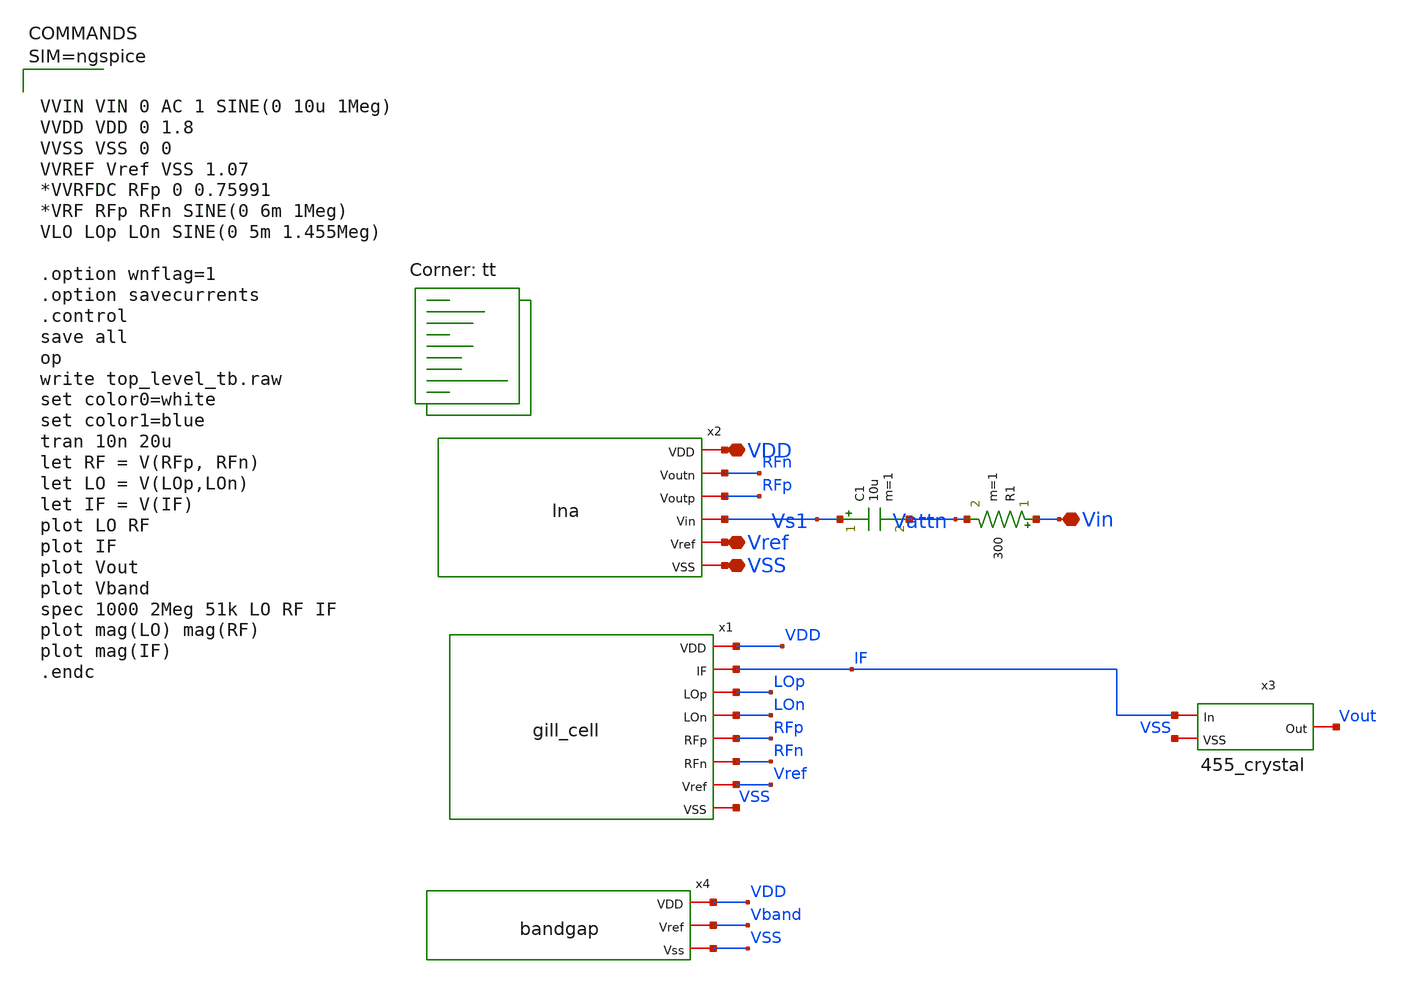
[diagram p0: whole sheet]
** sch_path: Project/xschem/top _level_tb.sch
**.subckt top _level_tb VDD Vin VSS Vref
*.iopin VDD
*.iopin Vin
*.iopin VSS
*.iopin Vref
x1 VDD IF LOp LOn RFp RFn Vref VSS gill_cell
C1 Vs1 Vattn 10u m=1
R1 Vin Vattn 300 m=1
x2 VDD RFn RFp Vs1 Vref VSS lna
x3 IF Vout VSS 455_crystal
x4 VDD Vband VSS bandgap
**** begin user architecture code



VVIN VIN 0 AC 1 SINE(0 10u 1Meg)
VVDD VDD 0 1.8
VVSS VSS 0 0
VVREF Vref VSS 1.07
*VVRFDC RFp 0 0.75991
*VRF RFp RFn SINE(0 6m 1Meg)
VLO LOp LOn SINE(0 5m 1.455Meg)

.option wnflag=1
.option savecurrents
.control
save all
op
write top_level_tb.raw
set color0=white
set color1=blue
tran 10n 20u
let RF = V(RFp, RFn)
let LO = V(LOp,LOn)
let IF = V(IF)
plot LO RF
plot IF
plot Vout
plot Vband
spec 1000 2Meg 51k LO RF IF
plot mag(LO) mag(RF)
plot mag(IF)
.endc



.lib $::SKYWATER_MODELS/sky130.lib.spice tt
**** end user architecture code
**.ends
.end
